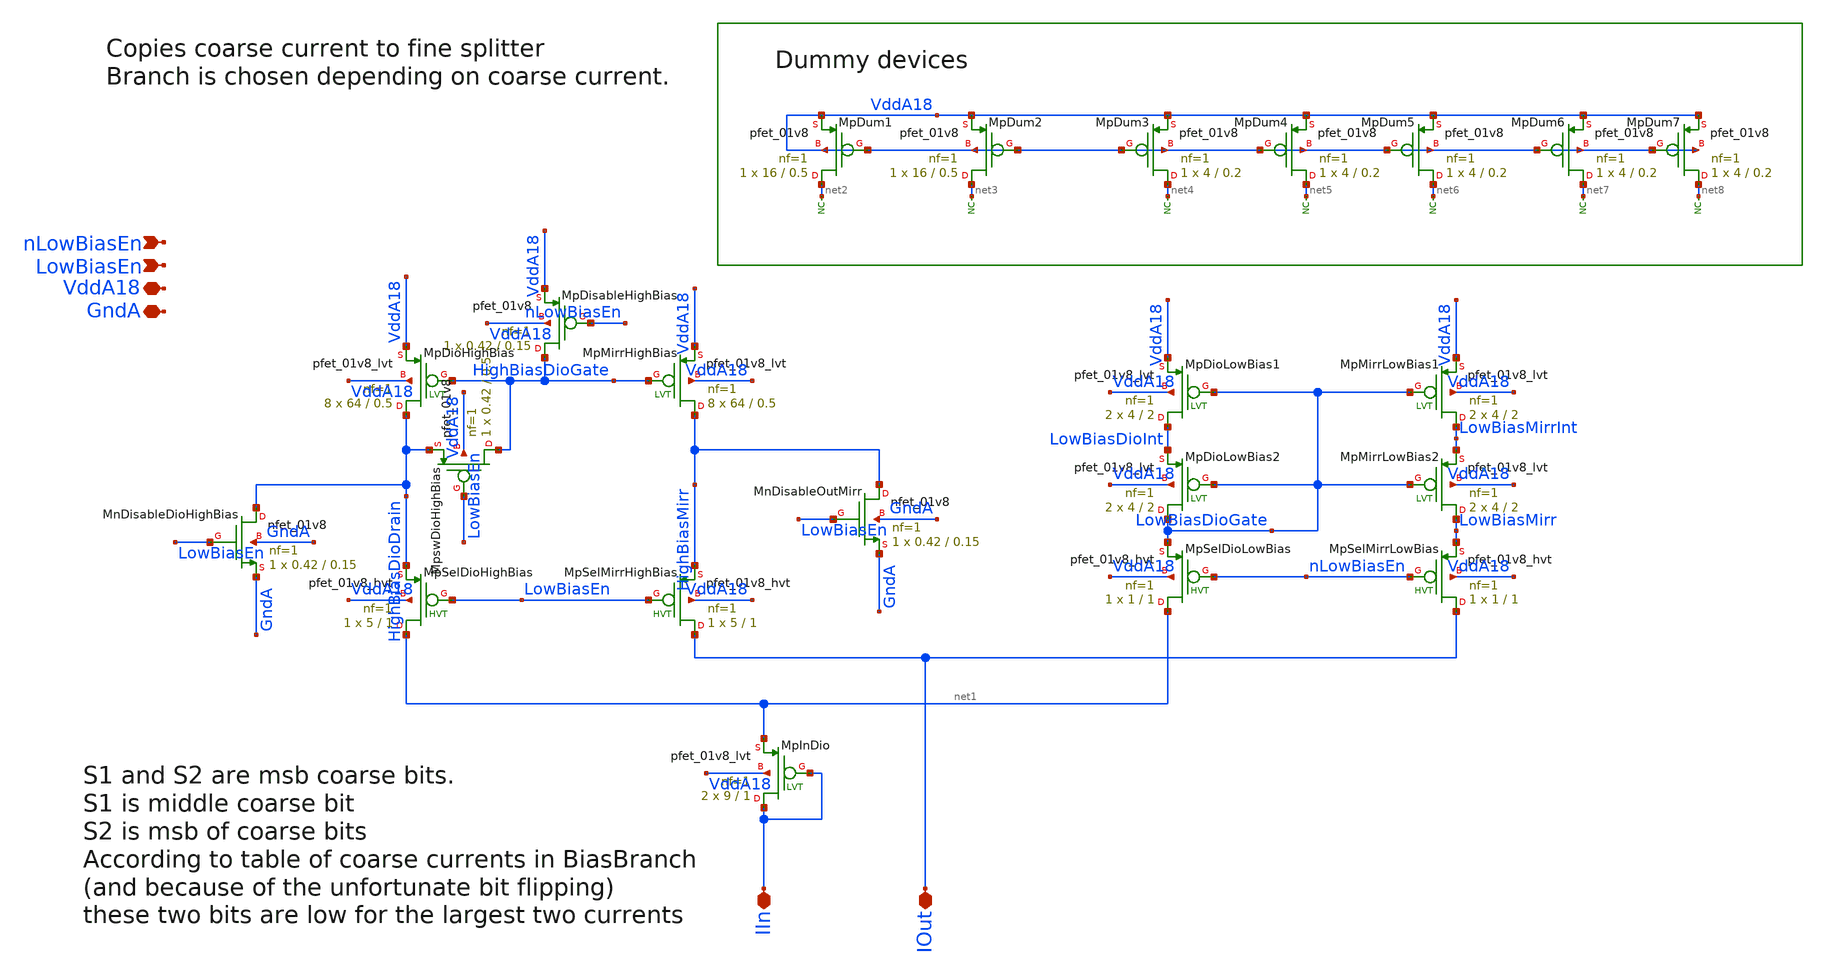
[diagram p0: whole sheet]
** sch_path: analog/xschem/BiasCoarseFineInterface_v1_bad_sizing.sch
**.subckt BiasCoarseFineInterface_v1_bad_sizing GndA VddA18 IIn IOut nLowBiasEn LowBiasEn
*.iopin GndA
*.iopin VddA18
*.iopin IIn
*.iopin IOut
*.ipin nLowBiasEn
*.ipin LowBiasEn
XMpDisableHighBias HighBiasDioGate nLowBiasEn VddA18 VddA18 sky130_fd_pr__pfet_01v8 L=0.15 W=0.42 nf=1
+ ad='int((1 + 1)/2) * 0.42 / 1 * 0.29' as='int((1 + 2)/2) * 0.42 / 1 * 0.29' pd='2*int((1 + 1)/2) * (0.42 / 1 + 0.29)'
+ ps='2*int((1 + 2)/2) * (0.42 / 1 + 0.29)' nrd='0.29 / 0.42 ' nrs='0.29 / 0.42 ' sa=0 sb=0 sd=0 mult=1
+ m=1
XMpDioHighBias HighBiasDioDrain HighBiasDioGate VddA18 VddA18 sky130_fd_pr__pfet_01v8_lvt L=0.5 W=64
+ nf=1 ad='int((1 + 1)/2) * 64 / 1 * 0.29' as='int((1 + 2)/2) * 64 / 1 * 0.29' pd='2*int((1 + 1)/2) * (64 / 1 + 0.29)'
+ ps='2*int((1 + 2)/2) * (64 / 1 + 0.29)' nrd='0.29 / 64 ' nrs='0.29 / 64 ' sa=0 sb=0 sd=0 mult=8 m=8
XMpMirrHighBias HighBiasMirr HighBiasDioGate VddA18 VddA18 sky130_fd_pr__pfet_01v8_lvt L=0.5 W=64 nf=1
+ ad='int((1 + 1)/2) * 64 / 1 * 0.29' as='int((1 + 2)/2) * 64 / 1 * 0.29' pd='2*int((1 + 1)/2) * (64 / 1 + 0.29)'
+ ps='2*int((1 + 2)/2) * (64 / 1 + 0.29)' nrd='0.29 / 64 ' nrs='0.29 / 64 ' sa=0 sb=0 sd=0 mult=8 m=8
XMpswDioHighBias HighBiasDioGate LowBiasEn HighBiasDioDrain VddA18 sky130_fd_pr__pfet_01v8 L=0.5 W=0.42
+ nf=1 ad='int((1 + 1)/2) * 0.42 / 1 * 0.29' as='int((1 + 2)/2) * 0.42 / 1 * 0.29' pd='2*int((1 + 1)/2) * (0.42 / 1 + 0.29)'
+ ps='2*int((1 + 2)/2) * (0.42 / 1 + 0.29)' nrd='0.29 / 0.42 ' nrs='0.29 / 0.42 ' sa=0 sb=0 sd=0 mult=1
+ m=1
XMnDisableDioHighBias HighBiasDioDrain LowBiasEn GndA GndA sky130_fd_pr__nfet_01v8 L=0.15 W=0.42 nf=1
+ ad='int((1 + 1)/2) * 0.42 / 1 * 0.29' as='int((1 + 2)/2) * 0.42 / 1 * 0.29' pd='2*int((1 + 1)/2) * (0.42 / 1 + 0.29)'
+ ps='2*int((1 + 2)/2) * (0.42 / 1 + 0.29)' nrd='0.29 / 0.42 ' nrs='0.29 / 0.42 ' sa=0 sb=0 sd=0 mult=1
+ m=1
XMpSelDioHighBias net1 LowBiasEn HighBiasDioDrain VddA18 sky130_fd_pr__pfet_01v8_hvt L=1 W=5 nf=1 ad='int((1 + 1)/2) * 5 / 1 * 0.29'
+ as='int((1 + 2)/2) * 5 / 1 * 0.29' pd='2*int((1 + 1)/2) * (5 / 1 + 0.29)' ps='2*int((1 + 2)/2) * (5 / 1 + 0.29)'
+ nrd='0.29 / 5 ' nrs='0.29 / 5 ' sa=0 sb=0 sd=0 mult=1 m=1
XMpSelMirrHighBias IOut LowBiasEn HighBiasMirr VddA18 sky130_fd_pr__pfet_01v8_hvt L=1 W=5 nf=1 ad='int((1 + 1)/2) * 5 / 1 * 0.29'
+ as='int((1 + 2)/2) * 5 / 1 * 0.29' pd='2*int((1 + 1)/2) * (5 / 1 + 0.29)' ps='2*int((1 + 2)/2) * (5 / 1 + 0.29)'
+ nrd='0.29 / 5 ' nrs='0.29 / 5 ' sa=0 sb=0 sd=0 mult=1 m=1
XMnDisableOutMirr HighBiasMirr LowBiasEn GndA GndA sky130_fd_pr__nfet_01v8 L=0.15 W=0.42 nf=1 ad='int((1 + 1)/2) * 0.42 / 1 * 0.29'
+ as='int((1 + 2)/2) * 0.42 / 1 * 0.29' pd='2*int((1 + 1)/2) * (0.42 / 1 + 0.29)' ps='2*int((1 + 2)/2) * (0.42 / 1 + 0.29)'
+ nrd='0.29 / 0.42 ' nrs='0.29 / 0.42 ' sa=0 sb=0 sd=0 mult=1 m=1
XMpInDio IIn IIn net1 VddA18 sky130_fd_pr__pfet_01v8_lvt L=1 W=9 nf=1 ad='int((1 + 1)/2) * 9 / 1 * 0.29'
+ as='int((1 + 2)/2) * 9 / 1 * 0.29' pd='2*int((1 + 1)/2) * (9 / 1 + 0.29)' ps='2*int((1 + 2)/2) * (9 / 1 + 0.29)'
+ nrd='0.29 / 9 ' nrs='0.29 / 9 ' sa=0 sb=0 sd=0 mult=2 m=2
XMpDioLowBias1 LowBiasDioInt LowBiasDioGate VddA18 VddA18 sky130_fd_pr__pfet_01v8_lvt L=2 W=4 nf=1 ad='int((1 + 1)/2) * 4 / 1 * 0.29'
+ as='int((1 + 2)/2) * 4 / 1 * 0.29' pd='2*int((1 + 1)/2) * (4 / 1 + 0.29)' ps='2*int((1 + 2)/2) * (4 / 1 + 0.29)'
+ nrd='0.29 / 4 ' nrs='0.29 / 4 ' sa=0 sb=0 sd=0 mult=2 m=2
XMpMirrLowBias1 LowBiasMirrInt LowBiasDioGate VddA18 VddA18 sky130_fd_pr__pfet_01v8_lvt L=2 W=4 nf=1
+ ad='int((1 + 1)/2) * 4 / 1 * 0.29' as='int((1 + 2)/2) * 4 / 1 * 0.29' pd='2*int((1 + 1)/2) * (4 / 1 + 0.29)'
+ ps='2*int((1 + 2)/2) * (4 / 1 + 0.29)' nrd='0.29 / 4 ' nrs='0.29 / 4 ' sa=0 sb=0 sd=0 mult=2 m=2
XMpDioLowBias2 LowBiasDioGate LowBiasDioGate LowBiasDioInt VddA18 sky130_fd_pr__pfet_01v8_lvt L=2 W=4
+ nf=1 ad='int((1 + 1)/2) * 4 / 1 * 0.29' as='int((1 + 2)/2) * 4 / 1 * 0.29' pd='2*int((1 + 1)/2) * (4 / 1 + 0.29)'
+ ps='2*int((1 + 2)/2) * (4 / 1 + 0.29)' nrd='0.29 / 4 ' nrs='0.29 / 4 ' sa=0 sb=0 sd=0 mult=2 m=2
XMpMirrLowBias2 LowBiasMirr LowBiasDioGate LowBiasMirrInt VddA18 sky130_fd_pr__pfet_01v8_lvt L=2 W=4
+ nf=1 ad='int((1 + 1)/2) * 4 / 1 * 0.29' as='int((1 + 2)/2) * 4 / 1 * 0.29' pd='2*int((1 + 1)/2) * (4 / 1 + 0.29)'
+ ps='2*int((1 + 2)/2) * (4 / 1 + 0.29)' nrd='0.29 / 4 ' nrs='0.29 / 4 ' sa=0 sb=0 sd=0 mult=2 m=2
XMpSelDioLowBias net1 nLowBiasEn LowBiasDioGate VddA18 sky130_fd_pr__pfet_01v8_hvt L=1 W=1 nf=1 ad='int((1 + 1)/2) * 1 / 1 * 0.29'
+ as='int((1 + 2)/2) * 1 / 1 * 0.29' pd='2*int((1 + 1)/2) * (1 / 1 + 0.29)' ps='2*int((1 + 2)/2) * (1 / 1 + 0.29)'
+ nrd='0.29 / 1 ' nrs='0.29 / 1 ' sa=0 sb=0 sd=0 mult=1 m=1
XMpSelMirrLowBias IOut nLowBiasEn LowBiasMirr VddA18 sky130_fd_pr__pfet_01v8_hvt L=1 W=1 nf=1 ad='int((1 + 1)/2) * 1 / 1 * 0.29'
+ as='int((1 + 2)/2) * 1 / 1 * 0.29' pd='2*int((1 + 1)/2) * (1 / 1 + 0.29)' ps='2*int((1 + 2)/2) * (1 / 1 + 0.29)'
+ nrd='0.29 / 1 ' nrs='0.29 / 1 ' sa=0 sb=0 sd=0 mult=1 m=1
XMpDum1 net2 VddA18 VddA18 VddA18 sky130_fd_pr__pfet_01v8 L=0.5 W=16 nf=1 ad='int((1 + 1)/2) * 16 / 1 * 0.29'
+ as='int((1 + 2)/2) * 16 / 1 * 0.29' pd='2*int((1 + 1)/2) * (16 / 1 + 0.29)' ps='2*int((1 + 2)/2) * (16 / 1 + 0.29)'
+ nrd='0.29 / 16 ' nrs='0.29 / 16 ' sa=0 sb=0 sd=0 mult=1 m=1
XMpDum2 net3 VddA18 VddA18 VddA18 sky130_fd_pr__pfet_01v8 L=0.5 W=16 nf=1 ad='int((1 + 1)/2) * 16 / 1 * 0.29'
+ as='int((1 + 2)/2) * 16 / 1 * 0.29' pd='2*int((1 + 1)/2) * (16 / 1 + 0.29)' ps='2*int((1 + 2)/2) * (16 / 1 + 0.29)'
+ nrd='0.29 / 16 ' nrs='0.29 / 16 ' sa=0 sb=0 sd=0 mult=1 m=1
XMpDum3 net4 VddA18 VddA18 VddA18 sky130_fd_pr__pfet_01v8 L=0.2 W=4 nf=1 ad='int((1 + 1)/2) * 4 / 1 * 0.29'
+ as='int((1 + 2)/2) * 4 / 1 * 0.29' pd='2*int((1 + 1)/2) * (4 / 1 + 0.29)' ps='2*int((1 + 2)/2) * (4 / 1 + 0.29)'
+ nrd='0.29 / 4 ' nrs='0.29 / 4 ' sa=0 sb=0 sd=0 mult=1 m=1
XMpDum4 net5 VddA18 VddA18 VddA18 sky130_fd_pr__pfet_01v8 L=0.2 W=4 nf=1 ad='int((1 + 1)/2) * 4 / 1 * 0.29'
+ as='int((1 + 2)/2) * 4 / 1 * 0.29' pd='2*int((1 + 1)/2) * (4 / 1 + 0.29)' ps='2*int((1 + 2)/2) * (4 / 1 + 0.29)'
+ nrd='0.29 / 4 ' nrs='0.29 / 4 ' sa=0 sb=0 sd=0 mult=1 m=1
XMpDum5 net6 VddA18 VddA18 VddA18 sky130_fd_pr__pfet_01v8 L=0.2 W=4 nf=1 ad='int((1 + 1)/2) * 4 / 1 * 0.29'
+ as='int((1 + 2)/2) * 4 / 1 * 0.29' pd='2*int((1 + 1)/2) * (4 / 1 + 0.29)' ps='2*int((1 + 2)/2) * (4 / 1 + 0.29)'
+ nrd='0.29 / 4 ' nrs='0.29 / 4 ' sa=0 sb=0 sd=0 mult=1 m=1
XMpDum6 net7 VddA18 VddA18 VddA18 sky130_fd_pr__pfet_01v8 L=0.2 W=4 nf=1 ad='int((1 + 1)/2) * 4 / 1 * 0.29'
+ as='int((1 + 2)/2) * 4 / 1 * 0.29' pd='2*int((1 + 1)/2) * (4 / 1 + 0.29)' ps='2*int((1 + 2)/2) * (4 / 1 + 0.29)'
+ nrd='0.29 / 4 ' nrs='0.29 / 4 ' sa=0 sb=0 sd=0 mult=1 m=1
XMpDum7 net8 VddA18 VddA18 VddA18 sky130_fd_pr__pfet_01v8 L=0.2 W=4 nf=1 ad='int((1 + 1)/2) * 4 / 1 * 0.29'
+ as='int((1 + 2)/2) * 4 / 1 * 0.29' pd='2*int((1 + 1)/2) * (4 / 1 + 0.29)' ps='2*int((1 + 2)/2) * (4 / 1 + 0.29)'
+ nrd='0.29 / 4 ' nrs='0.29 / 4 ' sa=0 sb=0 sd=0 mult=1 m=1
* noconn #net2
* noconn #net3
* noconn #net4
* noconn #net5
* noconn #net6
* noconn #net7
* noconn #net8
**.ends
.end
